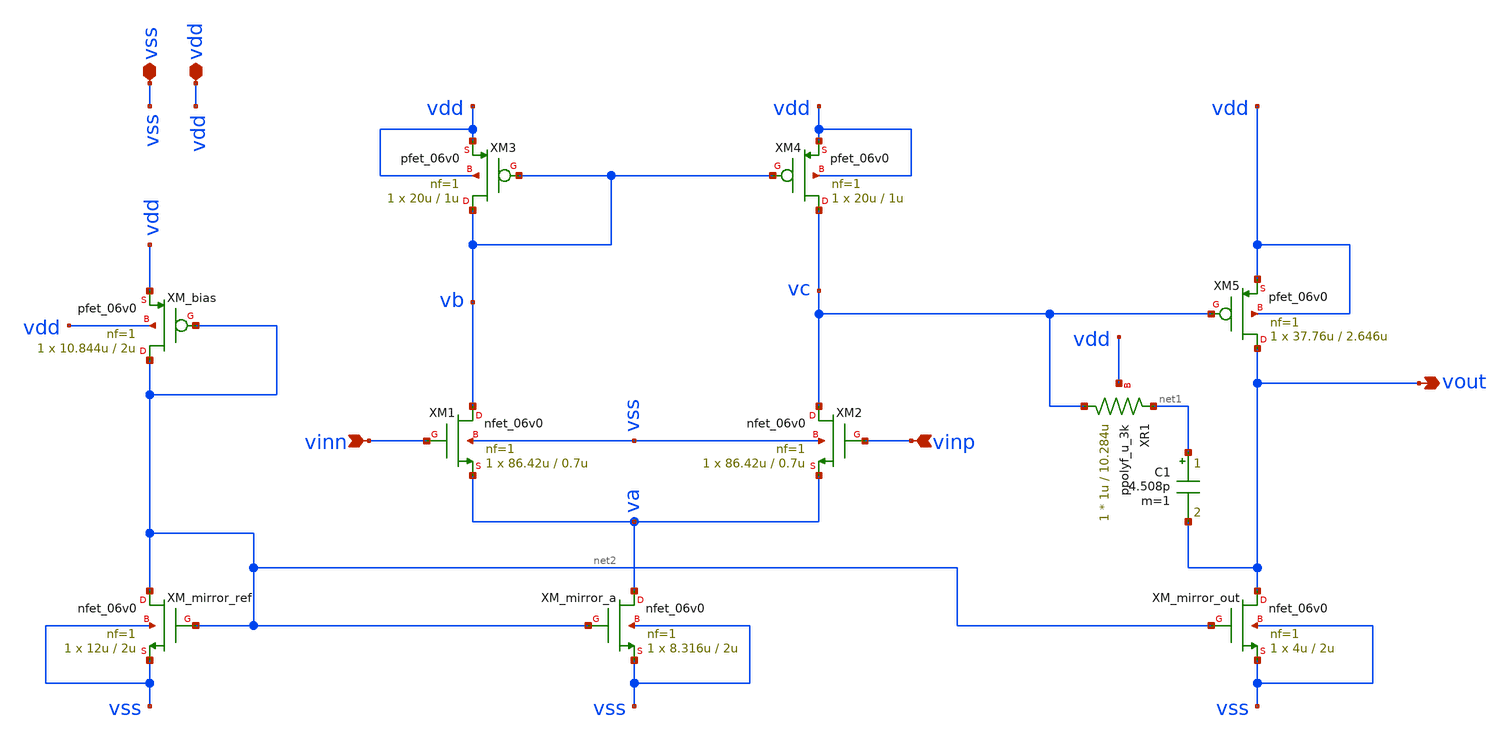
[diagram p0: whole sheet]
** sch_path: analog-db/drawings/ldo-005-ti-ldo-buffer-ref/gf180/ref_amp/ref_amp.sch
**.subckt ref_amp vinn vinp vdd vss vout
*.ipin vinn
*.ipin vinp
*.iopin vdd
*.iopin vss
*.opin vout
XM1 vb vinn va vss nfet_06v0 L=0.7u W=86.42u nf=1 ad='int((nf+1)/2) * W/nf * 0.18u' as='int((nf+2)/2) * W/nf * 0.18u'
+ pd='2*int((nf+1)/2) * (W/nf + 0.18u)' ps='2*int((nf+2)/2) * (W/nf + 0.18u)' nrd='0.18u / W' nrs='0.18u / W'
+ sa=0 sb=0 sd=0 m=1
XM2 vc vinp va vss nfet_06v0 L=0.7u W=86.42u nf=1 ad='int((nf+1)/2) * W/nf * 0.18u' as='int((nf+2)/2) * W/nf * 0.18u'
+ pd='2*int((nf+1)/2) * (W/nf + 0.18u)' ps='2*int((nf+2)/2) * (W/nf + 0.18u)' nrd='0.18u / W' nrs='0.18u / W'
+ sa=0 sb=0 sd=0 m=1
XM3 vb vb vdd vdd pfet_06v0 L=1u W=20u nf=1 ad='int((nf+1)/2) * W/nf * 0.18u' as='int((nf+2)/2) * W/nf * 0.18u'
+ pd='2*int((nf+1)/2) * (W/nf + 0.18u)' ps='2*int((nf+2)/2) * (W/nf + 0.18u)' nrd='0.18u / W' nrs='0.18u / W'
+ sa=0 sb=0 sd=0 m=1
XM4 vc vb vdd vdd pfet_06v0 L=1u W=20u nf=1 ad='int((nf+1)/2) * W/nf * 0.18u' as='int((nf+2)/2) * W/nf * 0.18u'
+ pd='2*int((nf+1)/2) * (W/nf + 0.18u)' ps='2*int((nf+2)/2) * (W/nf + 0.18u)' nrd='0.18u / W' nrs='0.18u / W'
+ sa=0 sb=0 sd=0 m=1
XM5 vout vc vdd vdd pfet_06v0 L=2.646u W=37.76u nf=1 ad='int((nf+1)/2) * W/nf * 0.18u' as='int((nf+2)/2) * W/nf * 0.18u'
+ pd='2*int((nf+1)/2) * (W/nf + 0.18u)' ps='2*int((nf+2)/2) * (W/nf + 0.18u)' nrd='0.18u / W' nrs='0.18u / W'
+ sa=0 sb=0 sd=0 m=1
C1 net1 vout 4.508p m=1
XR1 vc net1 vdd ppolyf_u_3k r_width=1u r_length=10.284u m=1
XM_mirror_a va net2 vss vss nfet_06v0 L=2u W=8.316u nf=1 ad='int((nf+1)/2) * W/nf * 0.18u' as='int((nf+2)/2) * W/nf * 0.18u'
+ pd='2*int((nf+1)/2) * (W/nf + 0.18u)' ps='2*int((nf+2)/2) * (W/nf + 0.18u)' nrd='0.18u / W' nrs='0.18u / W'
+ sa=0 sb=0 sd=0 m=1
XM_mirror_out vout net2 vss vss nfet_06v0 L=2u W=4u nf=1 ad='int((nf+1)/2) * W/nf * 0.18u' as='int((nf+2)/2) * W/nf * 0.18u'
+ pd='2*int((nf+1)/2) * (W/nf + 0.18u)' ps='2*int((nf+2)/2) * (W/nf + 0.18u)' nrd='0.18u / W' nrs='0.18u / W'
+ sa=0 sb=0 sd=0 m=1
XM_mirror_ref net2 net2 vss vss nfet_06v0 L=2u W=12u nf=1 ad='int((nf+1)/2) * W/nf * 0.18u' as='int((nf+2)/2) * W/nf * 0.18u'
+ pd='2*int((nf+1)/2) * (W/nf + 0.18u)' ps='2*int((nf+2)/2) * (W/nf + 0.18u)' nrd='0.18u / W' nrs='0.18u / W'
+ sa=0 sb=0 sd=0 m=1
XM_bias net2 net2 vdd vdd pfet_06v0 L=2u W=10.844u nf=1 ad='int((nf+1)/2) * W/nf * 0.18u' as='int((nf+2)/2) * W/nf * 0.18u'
+ pd='2*int((nf+1)/2) * (W/nf + 0.18u)' ps='2*int((nf+2)/2) * (W/nf + 0.18u)' nrd='0.18u / W' nrs='0.18u / W'
+ sa=0 sb=0 sd=0 m=1
**.ends
.end
